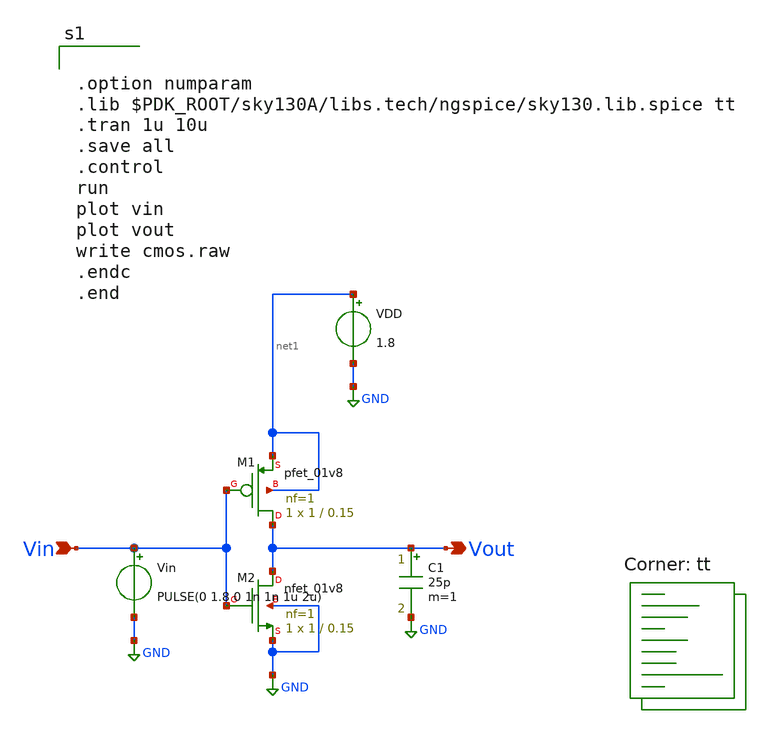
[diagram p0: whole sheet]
** sch_path: ANALOG/INVERTER/cmos.sch
**.subckt cmos Vin Vout
*.ipin Vin
*.opin Vout
XM1 Vout Vin net1 net1 sky130_fd_pr__pfet_01v8 L=0.15 W=1 nf=1 ad={int((nf+1)/2)*W/nf*0.29} as={int((nf+2)/2)*W/nf*0.29}
+ pd={2*int((nf+1)/2)*(W/nf+0.29)} ps={2*int((nf+2)/2)*(W/nf+0.29)} nrd={0.29/W} nrs={0.29/W} sa=0 sb=0
+ sd=0 mult=1 m=1
XM2 Vout Vin GND GND sky130_fd_pr__nfet_01v8 L=0.15 W=1 nf=1 ad={int((nf+1)/2)*W/nf*0.29} as={int((nf+2)/2)*W/nf*0.29}
+ pd={2*int((nf+1)/2)*(W/nf+0.29)} ps={2*int((nf+2)/2)*(W/nf+0.29)} nrd={0.29/W} nrs={0.29/W} sa=0 sb=0
+ sd=0 mult=1 m=1
Vin Vin GND PULSE(0 1.8 0 1n 1n 1u 2u)
VDD net1 GND 1.8
C1 Vout GND 25p m=1
**** begin user architecture code


.option numparam
.lib $PDK_ROOT/sky130A/libs.tech/ngspice/sky130.lib.spice tt
.tran 1u 10u
.save all
.control
run
plot vin
plot vout
write cmos.raw
.endc
.end



.lib $::SKYWATER_MODELS/sky130.lib.spice tt
**** end user architecture code
**.ends
.GLOBAL GND
.end
